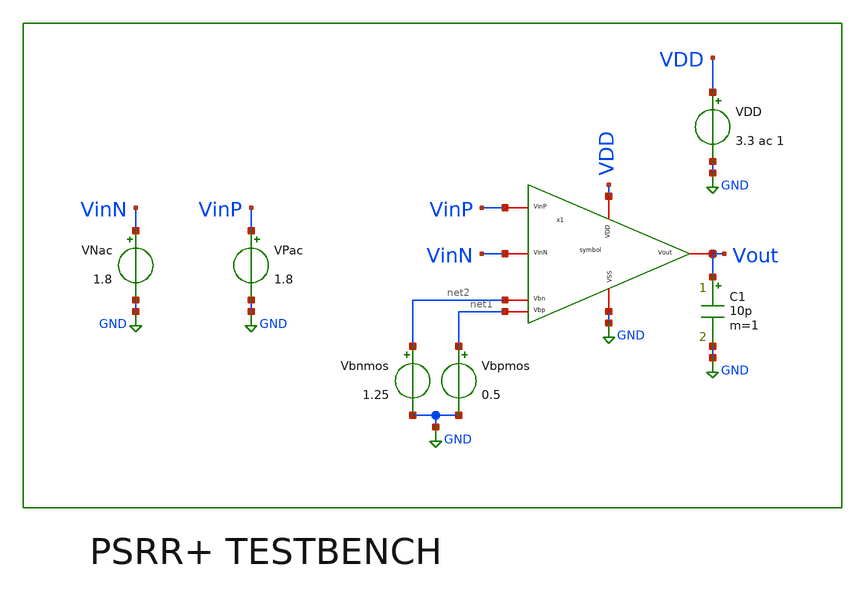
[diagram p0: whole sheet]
** sch_path: v2_bmr_bias/PSRR+.sch
**.subckt PSRR+
x1 VDD net1 VinP VinN Vout net2 GND symbol
VPac VinP GND 1.8
VNac VinN GND 1.8
Vbnmos net2 GND 1.25
Vbpmos net1 GND 0.5
VDD VDD GND 3.3 ac 1
C1 Vout GND 10p m=1
**** begin user architecture code


.control
close all
destroy all

ac dec 20 1 900Meg
let gain_vdd_db = db(Vout/VDD)
meas ac avdd_dc_gain find gain_vdd_db at=1

alter VPac ac = 100m
alter VNac ac = -100m
alter VDD ac = 0
ac dec 20 1 1000G
let VinDiff = v(VinP) - v(VinN)
let gain_dm_db = db(Vout/VinDiff)
meas ac adm_dc_gain find gain_dm_db at=1

let psrr_dc = adm_dc_gain - ac1.avdd_dc_gain
let psrr_full = gain_dm_db - ac1.gain_vdd_db

print adm_dc_gain
print ac1.avdd_dc_gain
print psrr_dc

plot ac1.gain_vdd_db gain_dm_db
plot psrr_full
.endc


**** end user architecture code
**.ends

* expanding   symbol:  /foss/designs/FOLDED/symbol.sym # of pins=7
** sym_path: v2_bmr_bias/symbol.sym
** sch_path: v2_bmr_bias/symbol.sch
.subckt symbol VDD Vbp VinP VinN Vout Vbn VSS
*.iopin Vbn
*.iopin Vbp
*.iopin VinP
*.iopin VinN
*.iopin Vout
*.iopin VDD
*.iopin VSS
XM1 net10 VinP net1 VSS sg13_hv_nmos w=7u l=1u ng=1 m=4 mm_ok=1
XM2 net9 VinN net1 VSS sg13_hv_nmos w=7u l=1u ng=1 m=4 mm_ok=1
XM3 net1 net3 VSS VSS sg13_hv_nmos w=3.75u l=1u ng=1 m=4 mm_ok=1
XM4 net10 net5 VDD VDD sg13_hv_pmos w=3.5u l=1u ng=1 m=4 mm_ok=1
XM5 net9 net5 VDD VDD sg13_hv_pmos w=3.5u l=1u ng=1 m=4 mm_ok=1
XM6 net2 Vbp net10 VDD sg13_hv_pmos w=4u l=1u ng=1 m=3 mm_ok=1
XM7 Vout Vbp net9 VDD sg13_hv_pmos w=4u l=1u ng=1 m=3 mm_ok=1
XM8 net2 Vbn net11 VSS sg13_hv_nmos w=7u l=1u ng=1 m=1 mm_ok=1
XM9 Vout Vbn net12 VSS sg13_hv_nmos w=7u l=1u ng=1 m=1 mm_ok=1
XM10 net11 net2 VSS VSS sg13_hv_nmos w=7u l=1u ng=1 m=1 mm_ok=1
XM11 net12 net2 VSS VSS sg13_hv_nmos w=7u l=1u ng=1 m=1 mm_ok=1
**** begin user architecture code



.lib cornerMOShv.lib mos_tt



**** end user architecture code
XM25 net3 net5 VDD VDD sg13_hv_pmos w=3.5u l=1u ng=1 m=1 mm_ok=1
XM12 net3 net3 VSS VSS sg13_hv_nmos w=3.75u l=1u ng=1 m=1 mm_ok=1
R1 net7 VSS 8.64k m=1
XM14 net8 net6 net7 VSS sg13_hv_nmos w=15u l=1u ng=2 m=1 mm_ok=1
XM15 net6 net6 VSS VSS sg13_hv_nmos w=3.75u l=1u ng=1 m=1 mm_ok=1
XM17 net6 net5 VDD VDD sg13_hv_pmos w=3.5u l=1u ng=1 m=1 mm_ok=1
XM18 net8 net5 VDD VDD sg13_hv_pmos w=3.5u l=1u ng=1 m=1 mm_ok=1
XM19 net4 net8 VSS VSS sg13_hv_nmos w=3.75u l=1u ng=1 m=1 mm_ok=1
XM20 net5 net6 VSS VSS sg13_hv_nmos w=3.75u l=1u ng=1 m=1 mm_ok=1
XM21 net4 net4 VDD VDD sg13_hv_pmos w=3.5u l=1u ng=1 m=1 mm_ok=1
XM22 net5 net4 VDD VDD sg13_hv_pmos w=3.5u l=1u ng=1 m=1 mm_ok=1
.ends

.GLOBAL GND
.end
